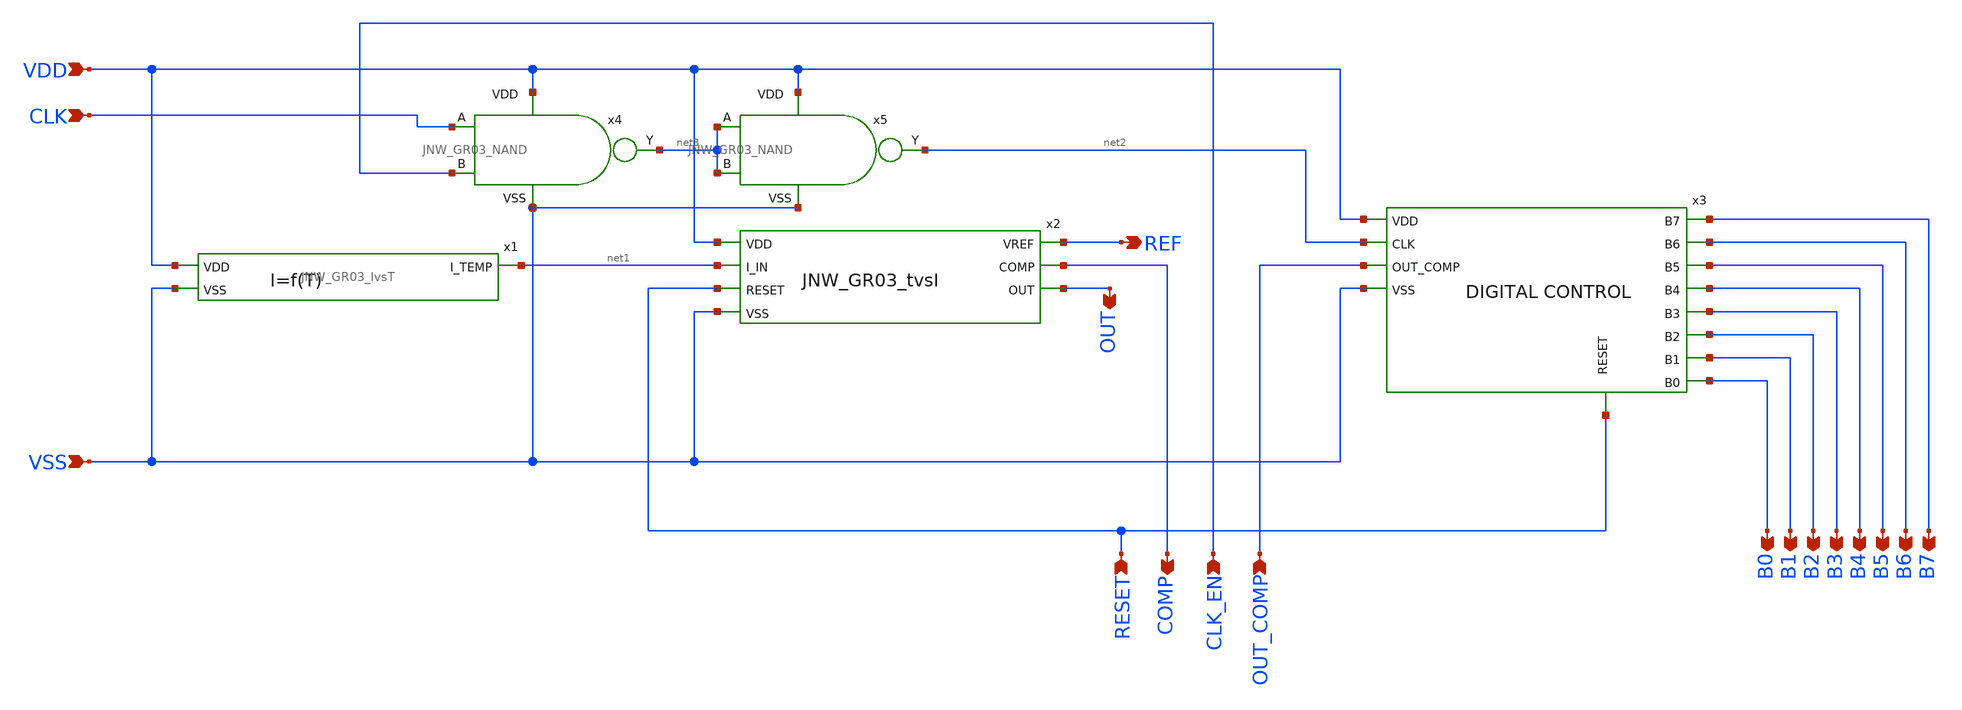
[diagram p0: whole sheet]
** sch_path: design/JNW_GR03_SKY130A/JNW_GR03.sch
**.subckt JNW_GR03 VDD VSS OUT COMP REF CLK B0 B1 B2 B3 B4 B5 B6 B7 RESET CLK_EN OUT_COMP
*.ipin VDD
*.ipin VSS
*.opin OUT
*.opin COMP
*.opin REF
*.ipin CLK
*.opin B0
*.opin B1
*.opin B2
*.opin B3
*.opin B4
*.opin B5
*.opin B6
*.opin B7
*.ipin RESET
*.ipin CLK_EN
*.ipin OUT_COMP
x1 VDD net1 VSS JNW_GR03_IvsT
x2 VDD net1 REF COMP OUT RESET VSS JNW_GR03_tvsI
x3 VDD net2 OUT_COMP VSS B1 B2 B0 B7 B3 B4 B6 B5 RESET JNW_GR03_DigitalControl
x4 VDD net3 CLK CLK_EN VSS JNW_GR03_NAND
x5 VDD net2 net3 net3 VSS JNW_GR03_NAND
**.ends
.end
